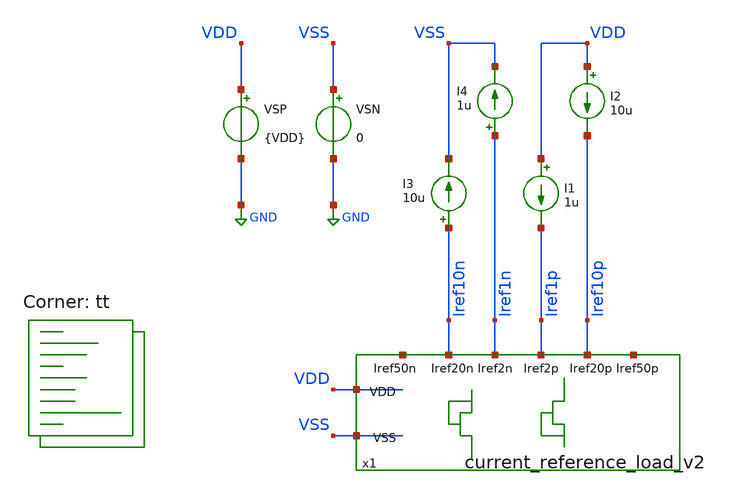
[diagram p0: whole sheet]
** sch_path: designs/libs/current_reference_load_v2/xschem/current_reference_load_v2_op.sch
**.subckt current_reference_load_v2_op
I4 Iref1n VSS 1u
VSN VSS GND 0
VSP VDD GND {VDD}
I1 VDD Iref1p 1u
I2 VDD Iref10p 10u
I3 Iref10n VSS 10u
x1 Iref1n net1 Iref1p net2 VDD VSS Iref10n Iref10p current_reference_load_v2
**** begin user architecture code
.lib $::SKYWATER_MODELS/sky130.lib.spice tt



.param VDD=1.8
.save

* Operation point of the loads given ideal current outputs from the CR

*nfet
  v(@m.x1.xm3.msky130_fd_pr__nfet_01v8[vds])  v(@m.x1.xm3.msky130_fd_pr__nfet_01v8[vth])
+  @m.x1.xm3.msky130_fd_pr__nfet_01v8[id]
  v(@m.x1.xm4.msky130_fd_pr__nfet_01v8[vds])  v(@m.x1.xm4.msky130_fd_pr__nfet_01v8[vth])
+  @m.x1.xm4.msky130_fd_pr__nfet_01v8[gds]

*pfet
  v(@m.x1.xm1.msky130_fd_pr__pfet_01v8_lvt[vds])  v(@m.x1.xm1.msky130_fd_pr__pfet_01v8_lvt[vth])
+  @m.x1.xm1.msky130_fd_pr__pfet_01v8_lvt[id]
  v(@m.x1.xm2.msky130_fd_pr__pfet_01v8_lvt[vds])  v(@m.x1.xm2.msky130_fd_pr__pfet_01v8_lvt[vth])
+  @m.x1.xm2.msky130_fd_pr__pfet_01v8_lvt[gds]
  abstol=1e-14 savecurrents
.control
    save all
    op
    write CR_loads_jangarita.raw

    print v(Iref10n) v(Iref1n) v(Iref1p) v(Iref10p)
.endc



**** end user architecture code
**.ends

* expanding   symbol:
*+  /foss/designs/chipathon_2025/designs/sky130/current_reference_load_v2/xschem/current_reference_load_v2.sym # of pins=8
** sym_path: designs/libs/current_reference_load_v2/xschem/current_reference_load_v2.sym
** sch_path: designs/libs/current_reference_load_v2/xschem/current_reference_load_v2.sch
.subckt current_reference_load_v2 Iref2n Iref50n Iref2p Iref50p VDD VSS Iref20n Iref20p
*.ipin Iref2n
*.iopin VDD
*.iopin VSS
*.ipin Iref50n
*.ipin Iref2p
*.ipin Iref50p
*.ipin Iref20p
*.ipin Iref20n
XM1 Iref2n Iref2n VDD VDD pfet_03v3 L=2u W=2u nf=1 ad='int((nf+1)/2) * W/nf * 0.18u' as='int((nf+2)/2) * W/nf * 0.18u'
+ pd='2*int((nf+1)/2) * (W/nf + 0.18u)' ps='2*int((nf+2)/2) * (W/nf + 0.18u)' nrd='0.18u / W' nrs='0.18u / W'
+ sa=0 sb=0 sd=0 m=2
XM4 Iref2p Iref2p VSS VSS nfet_03v3 L=2u W=4u nf=1 ad='int((nf+1)/2) * W/nf * 0.18u' as='int((nf+2)/2) * W/nf * 0.18u'
+ pd='2*int((nf+1)/2) * (W/nf + 0.18u)' ps='2*int((nf+2)/2) * (W/nf + 0.18u)' nrd='0.18u / W' nrs='0.18u / W'
+ sa=0 sb=0 sd=0 m=2
XM3 Iref50n Iref50n VDD VDD pfet_03v3 L=2u W=2u nf=1 ad='int((nf+1)/2) * W/nf * 0.18u' as='int((nf+2)/2) * W/nf * 0.18u'
+ pd='2*int((nf+1)/2) * (W/nf + 0.18u)' ps='2*int((nf+2)/2) * (W/nf + 0.18u)' nrd='0.18u / W' nrs='0.18u / W'
+ sa=0 sb=0 sd=0 m=50
XM6 Iref50p Iref50p VSS VSS nfet_03v3 L=2u W=4u nf=1 ad='int((nf+1)/2) * W/nf * 0.18u' as='int((nf+2)/2) * W/nf * 0.18u'
+ pd='2*int((nf+1)/2) * (W/nf + 0.18u)' ps='2*int((nf+2)/2) * (W/nf + 0.18u)' nrd='0.18u / W' nrs='0.18u / W'
+ sa=0 sb=0 sd=0 m=50
XM2 Iref20n Iref20n VDD VDD pfet_03v3 L=2u W=2u nf=1 ad='int((nf+1)/2) * W/nf * 0.18u' as='int((nf+2)/2) * W/nf * 0.18u'
+ pd='2*int((nf+1)/2) * (W/nf + 0.18u)' ps='2*int((nf+2)/2) * (W/nf + 0.18u)' nrd='0.18u / W' nrs='0.18u / W'
+ sa=0 sb=0 sd=0 m=20
XM5 Iref20p Iref20p VSS VSS nfet_03v3 L=2u W=4u nf=1 ad='int((nf+1)/2) * W/nf * 0.18u' as='int((nf+2)/2) * W/nf * 0.18u'
+ pd='2*int((nf+1)/2) * (W/nf + 0.18u)' ps='2*int((nf+2)/2) * (W/nf + 0.18u)' nrd='0.18u / W' nrs='0.18u / W'
+ sa=0 sb=0 sd=0 m=20
.ends

.GLOBAL GND
.end
